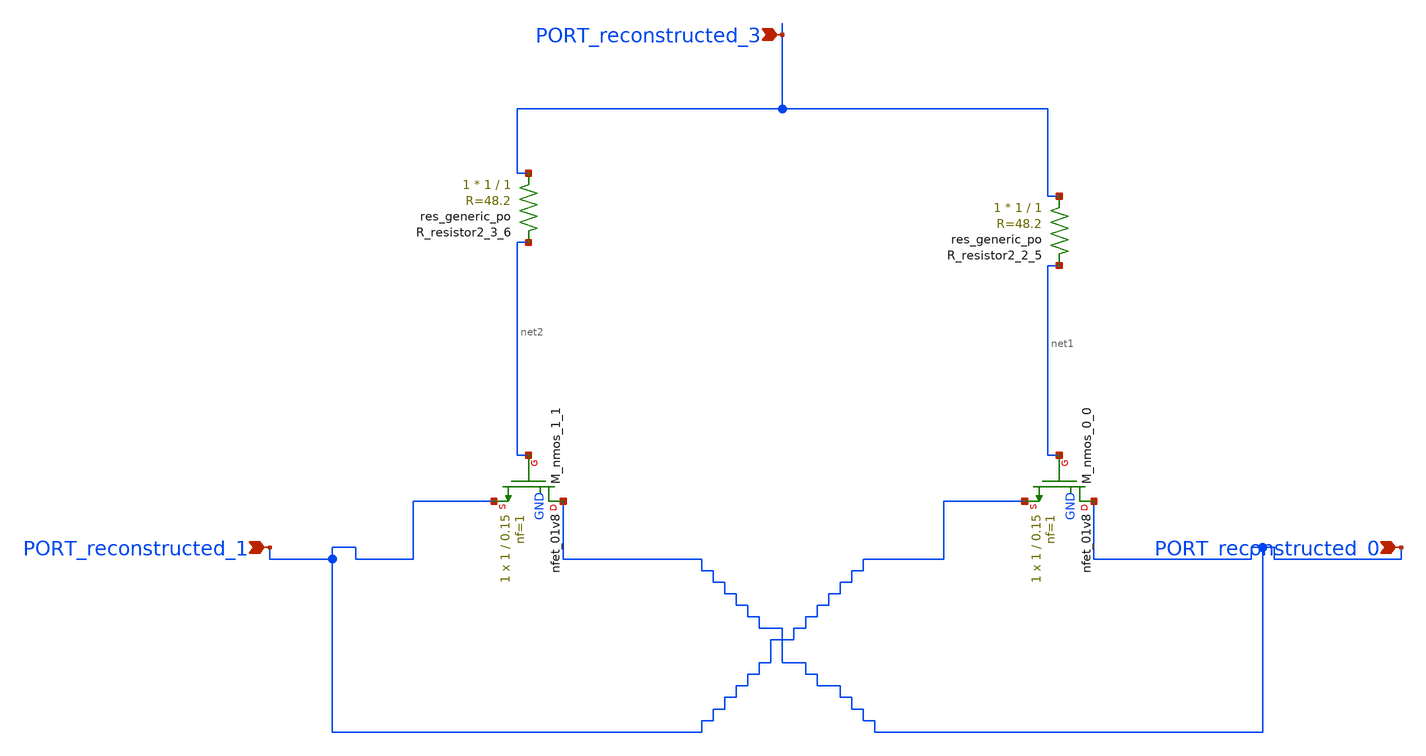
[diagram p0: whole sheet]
** sch_path: schematics/AMSNet/20.sch
**.subckt 20 PORT_reconstructed_3 PORT_reconstructed_0 PORT_reconstructed_1
*.ipin PORT_reconstructed_3
*.ipin PORT_reconstructed_0
*.ipin PORT_reconstructed_1
XM_nmos_0_0 PORT_reconstructed_0 net1 PORT_reconstructed_1 GND sky130_fd_pr__nfet_01v8 L=0.15 W=1 nf=1
+ ad='int((1 + 1)/2) * 1 / 1 * 0.29' as='int((1 + 2)/2) * 1 / 1 * 0.29' pd='2*int((1 + 1)/2) * (1 / 1 + 0.29)'
+ ps='2*int((1 + 2)/2) * (1 / 1 + 0.29)' nrd='0.29 / 1 ' nrs='0.29 / 1 ' sa=0 sb=0 sd=0 mult=1 m=1
XM_nmos_1_1 PORT_reconstructed_0 net2 PORT_reconstructed_1 GND sky130_fd_pr__nfet_01v8 L=0.15 W=1 nf=1
+ ad='int((1 + 1)/2) * 1 / 1 * 0.29' as='int((1 + 2)/2) * 1 / 1 * 0.29' pd='2*int((1 + 1)/2) * (1 / 1 + 0.29)'
+ ps='2*int((1 + 2)/2) * (1 / 1 + 0.29)' nrd='0.29 / 1 ' nrs='0.29 / 1 ' sa=0 sb=0 sd=0 mult=1 m=1
XR_resistor2_2_5 PORT_reconstructed_3 net1 sky130_fd_pr__res_generic_po W=1 L=1 m=1
XR_resistor2_3_6 PORT_reconstructed_3 net2 sky130_fd_pr__res_generic_po W=1 L=1 m=1
**.ends
.end
